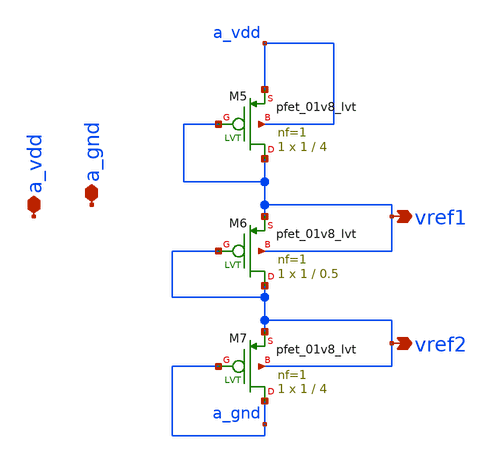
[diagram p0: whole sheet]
** sch_path: xschem/reference.sch
**.subckt reference a_vdd a_gnd vref1 vref2
*.iopin a_vdd
*.iopin a_gnd
*.opin vref1
*.opin vref2
XM5 vref1 vref1 a_vdd a_vdd sky130_fd_pr__pfet_01v8_lvt L=4 W=1 nf=1 ad='int((nf+1)/2) * W/nf * 0.29'
+ as='int((nf+2)/2) * W/nf * 0.29' pd='2*int((nf+1)/2) * (W/nf + 0.29)' ps='2*int((nf+2)/2) * (W/nf + 0.29)'
+ nrd='0.29 / W' nrs='0.29 / W' sa=0 sb=0 sd=0 mult=1 m=1
XM6 vref2 vref2 vref1 vref1 sky130_fd_pr__pfet_01v8_lvt L=0.5 W=1 nf=1 ad='int((nf+1)/2) * W/nf * 0.29'
+ as='int((nf+2)/2) * W/nf * 0.29' pd='2*int((nf+1)/2) * (W/nf + 0.29)' ps='2*int((nf+2)/2) * (W/nf + 0.29)'
+ nrd='0.29 / W' nrs='0.29 / W' sa=0 sb=0 sd=0 mult=1 m=1
XM7 a_gnd a_gnd vref2 vref2 sky130_fd_pr__pfet_01v8_lvt L=4 W=1 nf=1 ad='int((nf+1)/2) * W/nf * 0.29'
+ as='int((nf+2)/2) * W/nf * 0.29' pd='2*int((nf+1)/2) * (W/nf + 0.29)' ps='2*int((nf+2)/2) * (W/nf + 0.29)'
+ nrd='0.29 / W' nrs='0.29 / W' sa=0 sb=0 sd=0 mult=1 m=1
**.ends
.end
